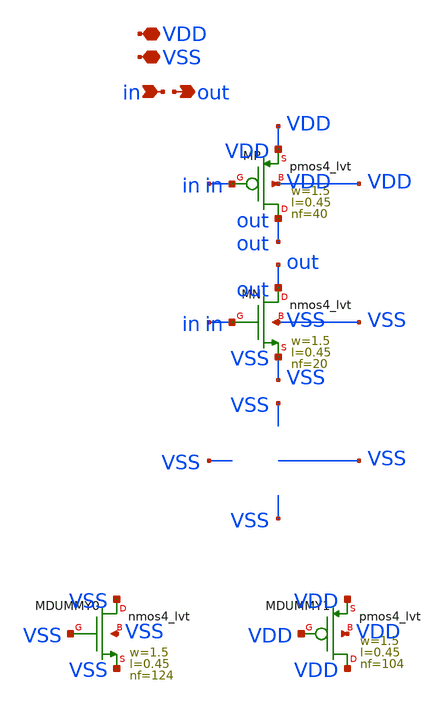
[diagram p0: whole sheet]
** sch_path: xschem/mux_2to1_generated_sky130_fd_pr/inverter2/inverter2.sch
**.subckt inverter2 VDD VSS in out
*.iopin VDD
*.iopin VSS
*.ipin in
*.opin out
XMN out in VSS VSS nmos4_lvt w=1.5 l=0.45 nf=20
XMP out in VDD VDD pmos4_lvt w=1.5 l=0.45 nf=40
XMDUMMY0 VSS VSS VSS VSS nmos4_lvt w=1.5 l=0.45 nf=124
XMDUMMY1 VDD VDD VDD VDD pmos4_lvt w=1.5 l=0.45 nf=104
**.ends

* expanding   symbol:  mux_2to1_generated_sky130_fd_pr/BAG_prim/nmos4_lvt/nmos4_lvt.sym # of pins=4
** sym_path: xschem/mux_2to1_generated_sky130_fd_pr/BAG_prim/nmos4_lvt/nmos4_lvt.sym
** sch_path: xschem/mux_2to1_generated_sky130_fd_pr/BAG_prim/nmos4_lvt/nmos4_lvt.sch
.subckt nmos4_lvt D G S B model
w=100n
l=18n
nf=4
model=nmos4_lvt


*.iopin D
*.iopin G
*.iopin S
*.iopin B
MM1 D G S B sky130_fd_pr__nfet_01v8_lvt L=l W='w * nf ' nf=nf ad='int((nf+1)/2) * W * 0.29u' as='int((nf+2)/2) * W * 0.29u'
+ pd='2*int((nf+1)/2) * (W + 0.29u)' ps='2*int((nf+2)/2) * (W + 0.29u)' nrd='0.29u*nf / W' nrs='0.29u*nf / W'
+ sa=0 sb=0 sd=0 mult=1 m=1
.ends


* expanding   symbol:  mux_2to1_generated_sky130_fd_pr/BAG_prim/pmos4_lvt/pmos4_lvt.sym # of pins=4
** sym_path: xschem/mux_2to1_generated_sky130_fd_pr/BAG_prim/pmos4_lvt/pmos4_lvt.sym
** sch_path: xschem/mux_2to1_generated_sky130_fd_pr/BAG_prim/pmos4_lvt/pmos4_lvt.sch
.subckt pmos4_lvt D G S B model
w=100n
l=18n
nf=4
model=pmos4_lvt


*.iopin D
*.iopin G
*.iopin S
*.iopin B
MM1 D G S B sky130_fd_pr__pfet_01v8_lvt L=l W='w * nf ' nf=nf ad='int((nf+1)/2) * W * 0.29u' as='int((nf+2)/2) * W * 0.29u'
+ pd='2*int((nf+1)/2) * (W + 0.29u)' ps='2*int((nf+2)/2) * (W + 0.29u)' nrd='0.29u*nf / W' nrs='0.29u*nf / W'
+ sa=0 sb=0 sd=0 mult=1 m=1
.ends

.end
